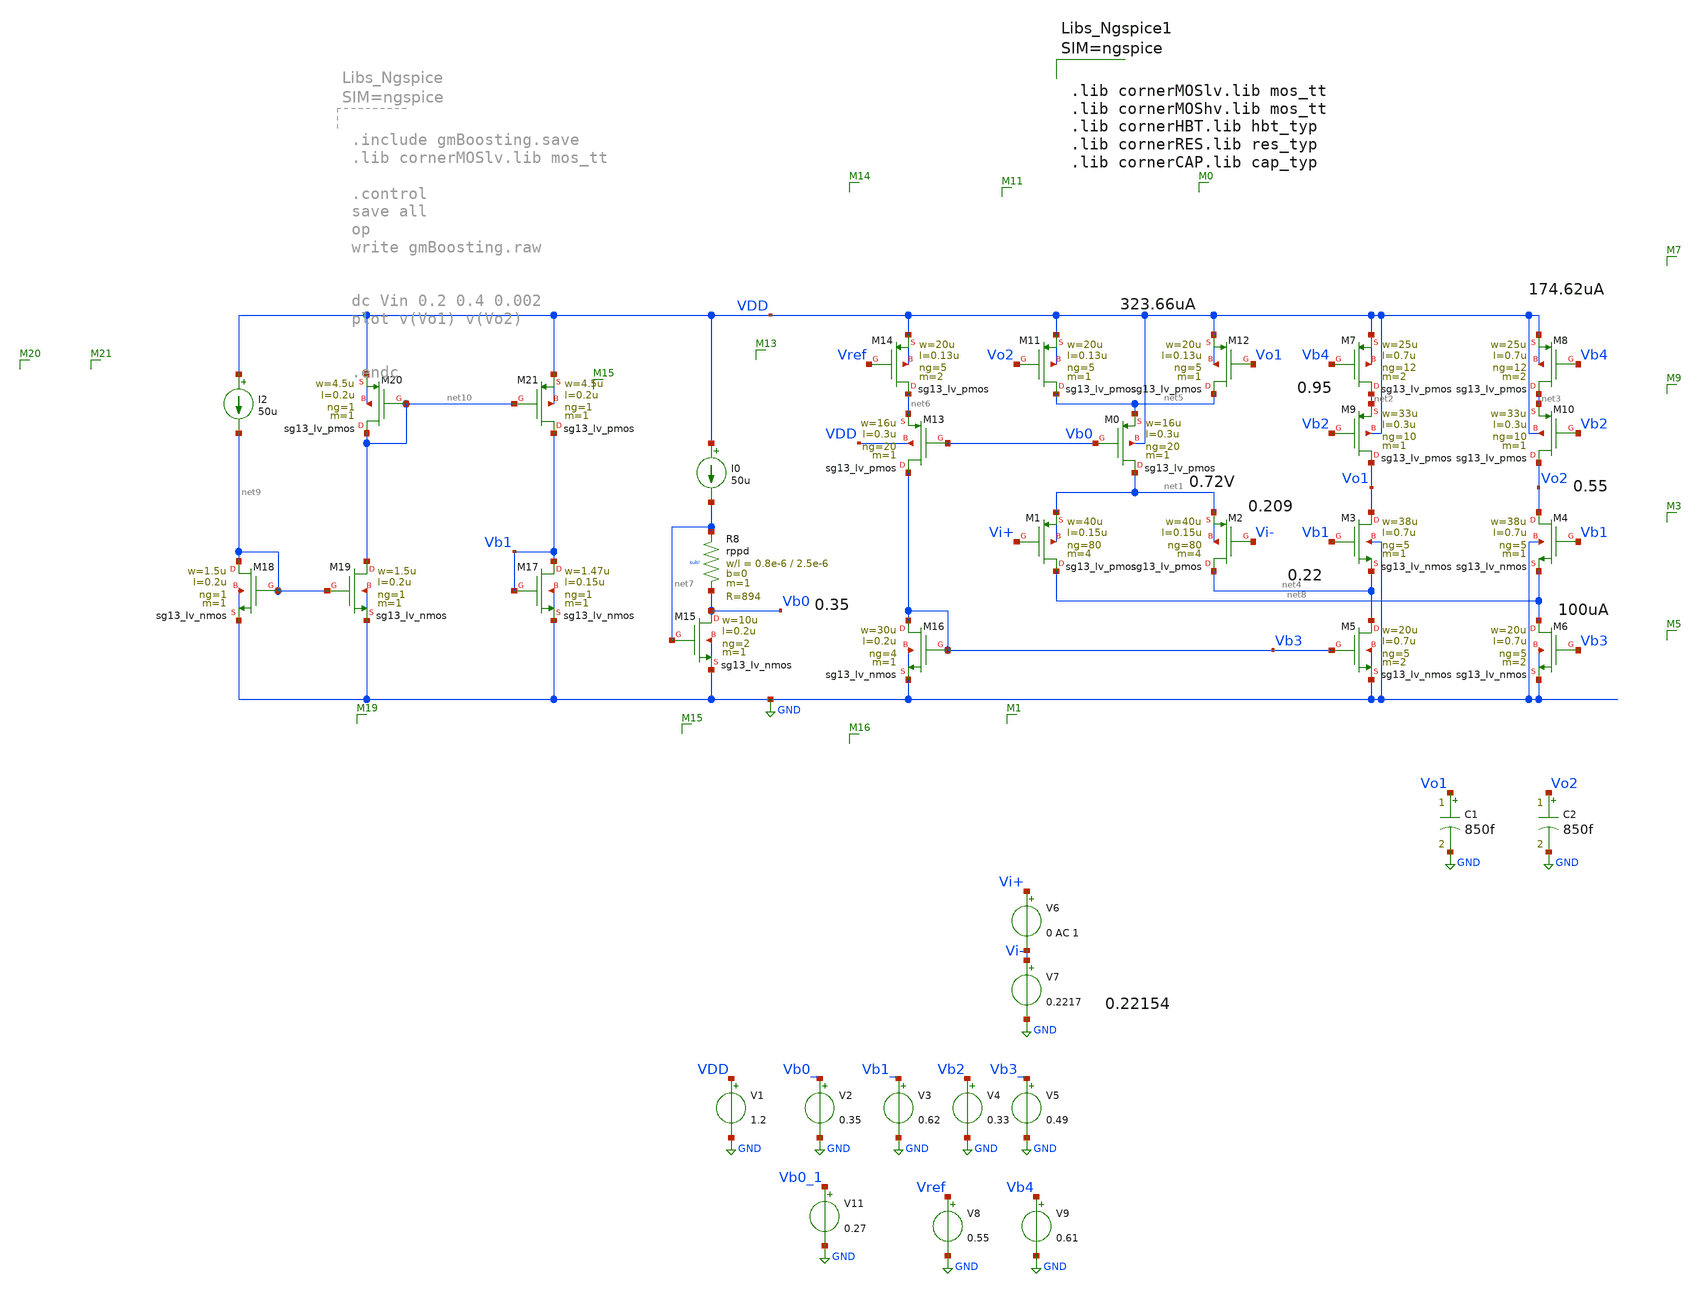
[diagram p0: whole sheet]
** sch_path: sch/testing/gmBoosting.sch
**.subckt gmBoosting
XM7 net2 Vb4 VDD VDD sg13_lv_pmos w=25u l=0.7u ng=12 m=2 mm_ok=1
XM1 net8 Vi+ net1 net1 sg13_lv_pmos w=40u l=0.15u ng=80 m=4 mm_ok=1
XM2 net4 Vi- net1 net1 sg13_lv_pmos w=40u l=0.15u ng=80 m=4 mm_ok=1
XM0 net1 Vb0 net5 VDD sg13_lv_pmos w=16u l=0.3u ng=20 m=1 mm_ok=1
XM6 net8 Vb3 GND GND sg13_lv_nmos w=20u l=0.7u ng=5 m=2 mm_ok=1
V1 VDD GND 1.2
V2 Vb0_ GND 0.35
V3 Vb1_ GND 0.62
V4 Vb2 GND 0.33
V5 Vb3_ GND 0.49
V7 Vi- GND 0.2217
V6 Vi+ Vi- 0 AC 1
C1 Vo1 GND 850f m=1
C2 Vo2 GND 850f m=1
XM9 Vo1 Vb2 net2 VDD sg13_lv_pmos w=33u l=0.3u ng=10 m=1 mm_ok=1
XM10 Vo2 Vb2 net3 VDD sg13_lv_pmos w=33u l=0.3u ng=10 m=1 mm_ok=1
V9 Vb4 GND 0.61
XM8 net3 Vb4 VDD VDD sg13_lv_pmos w=25u l=0.7u ng=12 m=2 mm_ok=1
V11 Vb0_1 GND 0.27
XM11 net5 Vo2 VDD VDD sg13_lv_pmos w=20u l=0.13u ng=5 m=1 mm_ok=1
XM12 net5 Vo1 VDD VDD sg13_lv_pmos w=20u l=0.13u ng=5 m=1 mm_ok=1
XM14 net6 Vref VDD VDD sg13_lv_pmos w=20u l=0.13u ng=5 m=2 mm_ok=1
V8 Vref GND 0.55
XM15 Vb0 net7 GND GND sg13_lv_nmos w=10u l=0.2u ng=2 m=1 mm_ok=1
XM16 Vb3 Vb3 GND GND sg13_lv_nmos w=30u l=0.2u ng=4 m=1 mm_ok=1
I0 VDD net7 50u
XR8 net7 Vb0 sub! rppd w=0.8e-6 l=2.5e-6 m=1 b=0 mm_ok=1
XM13 Vb3 Vb0 net6 VDD sg13_lv_pmos w=16u l=0.3u ng=20 m=1 mm_ok=1
XM5 net4 Vb3 GND GND sg13_lv_nmos w=20u l=0.7u ng=5 m=2 mm_ok=1
XM3 Vo1 Vb1 net4 GND sg13_lv_nmos w=38u l=0.7u ng=5 m=1 mm_ok=1
XM4 Vo2 Vb1 net8 GND sg13_lv_nmos w=38u l=0.7u ng=5 m=1 mm_ok=1
XM17 Vb1 Vb1 GND GND sg13_lv_nmos w=1.47u l=0.15u ng=1 m=1 mm_ok=1
I2 VDD net9 50u
XM18 net9 net9 GND GND sg13_lv_nmos w=1.5u l=0.2u ng=1 m=1 mm_ok=1
XM19 net10 net9 GND GND sg13_lv_nmos w=1.5u l=0.2u ng=1 m=1 mm_ok=1
XM20 net10 net10 VDD VDD sg13_lv_pmos w=4.5u l=0.2u ng=1 m=1 mm_ok=1
XM21 Vb1 net10 VDD VDD sg13_lv_pmos w=4.5u l=0.2u ng=1 m=1 mm_ok=1
**** begin user architecture code



.lib cornerMOSlv.lib mos_tt
.lib cornerMOShv.lib mos_tt
.lib cornerHBT.lib hbt_typ
.lib cornerRES.lib res_typ
.lib cornerCAP.lib cap_typ






.include gmBoosting.save
.lib cornerMOSlv.lib mos_tt
.temp 65
.control
save all
op
write gmBoosting.raw


ac dec 1k 1 10G
let Av = db((v(Vo1)-v(Vo2)))
meas ac UGBW WHEN Av=0
let phase_vec = 180/pi*cph(v(Vo1)-v(Vo2))

meas ac phase FIND phase_vec WHEN frequency=UGBW
let PM = phase+180
print PM

plot Av
plot phase_vec



.endc



**** end user architecture code
**.ends
.GLOBAL GND
.end
